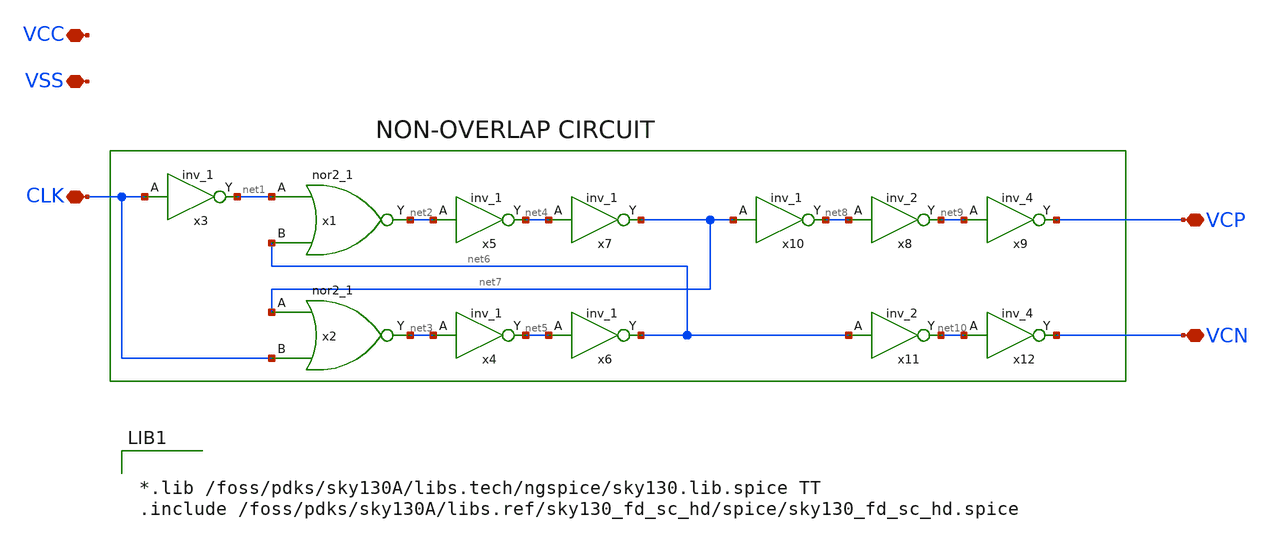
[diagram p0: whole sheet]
** sch_path: xschem/NOL_v1p1.sch
**.subckt NOL_v1p1 CLK VCP VCN VCC VSS
*.iopin CLK
*.iopin VCP
*.iopin VCN
*.iopin VCC
*.iopin VSS
x3 CLK VSS VSS VCC VCC net1 sky130_fd_sc_hd__inv_1
x4 net3 VSS VSS VCC VCC net5 sky130_fd_sc_hd__inv_1
x5 net2 VSS VSS VCC VCC net4 sky130_fd_sc_hd__inv_1
x1 net1 net6 VSS VSS VCC VCC net2 sky130_fd_sc_hd__nor2_1
x2 net7 CLK VSS VSS VCC VCC net3 sky130_fd_sc_hd__nor2_1
x6 net5 VSS VSS VCC VCC net6 sky130_fd_sc_hd__inv_1
x7 net4 VSS VSS VCC VCC net7 sky130_fd_sc_hd__inv_1
x8 net8 VSS VSS VCC VCC net9 sky130_fd_sc_hd__inv_2
x9 net9 VSS VSS VCC VCC VCP sky130_fd_sc_hd__inv_4
x10 net7 VSS VSS VCC VCC net8 sky130_fd_sc_hd__inv_1
x11 net6 VSS VSS VCC VCC net10 sky130_fd_sc_hd__inv_2
x12 net10 VSS VSS VCC VCC VCN sky130_fd_sc_hd__inv_4
**** begin user architecture code


*.lib /foss/pdks/sky130A/libs.tech/ngspice/sky130.lib.spice TT
.include /foss/pdks/sky130A/libs.ref/sky130_fd_sc_hd/spice/sky130_fd_sc_hd.spice


**** end user architecture code
**.ends
.end
